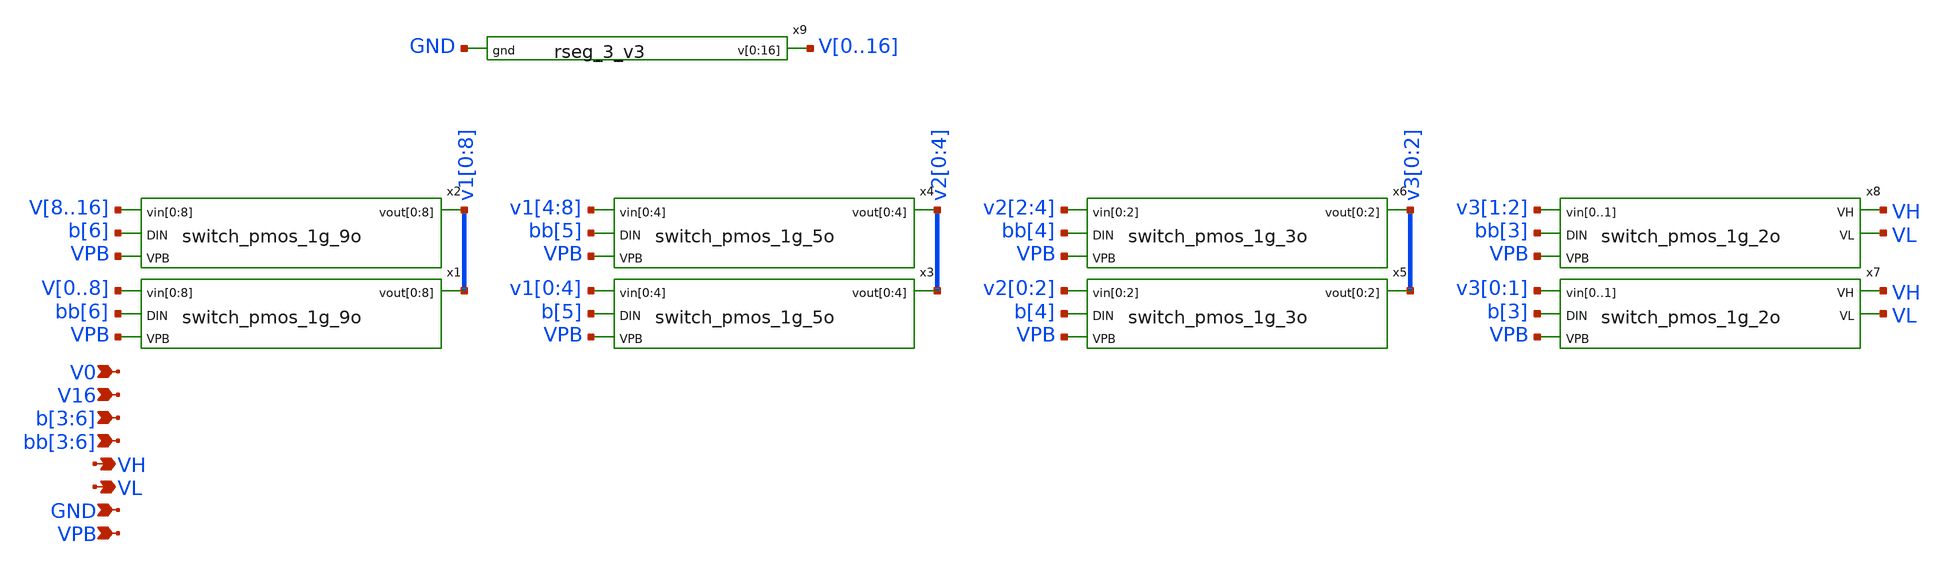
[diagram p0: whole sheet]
** sch_path: xschem/top_segment_3.sch
**.subckt top_segment_3 VH VPB b[3],b[4],b[5],b[6] VL bb[3],bb[4],bb[5],bb[6] V16 V0 GND
*.opin VH
*.ipin VPB
*.ipin b[3],b[4],b[5],b[6]
*.opin VL
*.ipin bb[3],bb[4],bb[5],bb[6]
*.ipin V16
*.ipin V0
*.ipin GND
x1 V0 V1 V2 V3 V4 V5 V6 V7 V8 bb[6] v1[0] v1[1] v1[2] v1[3] v1[4] v1[5] v1[6] v1[7] v1[8] VPB
+ switch_pmos_1g_9o
x2 V8 V9 V10 V11 V12 V13 V14 V15 V16 b[6] v1[0] v1[1] v1[2] v1[3] v1[4] v1[5] v1[6] v1[7] v1[8] VPB
+ switch_pmos_1g_9o
x3 v1[0] v1[1] v1[2] v1[3] v1[4] b[5] v2[0] v2[1] v2[2] v2[3] v2[4] VPB switch_pmos_1g_5o
x4 v1[4] v1[5] v1[6] v1[7] v1[8] bb[5] v2[0] v2[1] v2[2] v2[3] v2[4] VPB switch_pmos_1g_5o
x5 v2[0] v2[1] v2[2] b[4] v3[0] v3[1] v3[2] VPB switch_pmos_1g_3o
x6 v2[2] v2[3] v2[4] bb[4] v3[0] v3[1] v3[2] VPB switch_pmos_1g_3o
x7 v3[0] v3[1] b[3] VH VL VPB switch_pmos_1g_2o
x8 v3[1] v3[2] bb[3] VH VL VPB switch_pmos_1g_2o
x9 V0 V1 V2 V3 V4 V5 V6 V7 V8 V9 V10 V11 V12 V13 V14 V15 V16 GND rseg_3_v3
**.ends
.end
